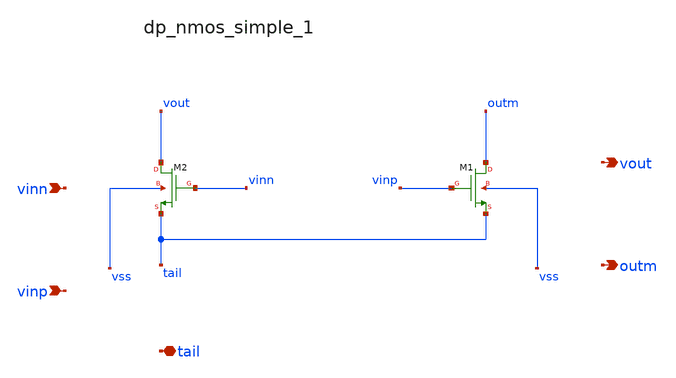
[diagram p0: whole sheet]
** sch_path: analog-db/raw/amp_001_5t/hier/blocks/dp_nmos_simple_1.sch
**.subckt dp_nmos_simple_1 vinn vinp tail vout outm
*.ipin vinn
*.ipin vinp
*.iopin tail
*.opin vout
*.opin outm
XM1 outm vinp tail vss sg13_lv_nmos w=x_dut_xm1_w l=x_dut_xm1_l ng=1 m=x_dut_xm1_m
XM2 vout vinn tail vss sg13_lv_nmos w=x_dut_xm2_w l=x_dut_xm2_l ng=1 m=x_dut_xm2_m
**.ends
.end
